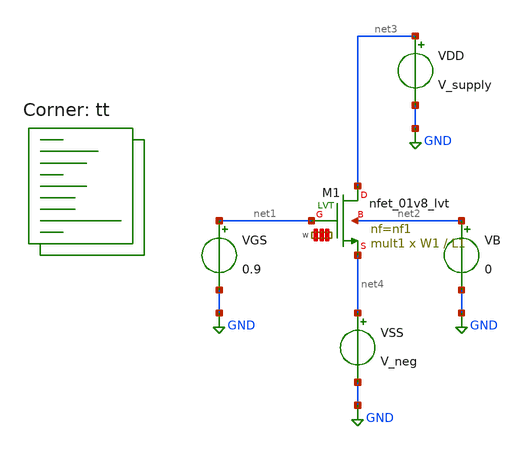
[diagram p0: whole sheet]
** sch_path: automatization_analog_design/mos_dc_characteristic/test.sch
**.subckt test
XM1 net3 net1 net4 net2 sky130_fd_pr__nfet_01v8_lvt L=L1 W='W1 * nf1 ' nf=nf1 ad='int((nf1 + 1)/2) * W1 / nf1 * 0.29'
+ as='int((nf1 + 2)/2) * W1 / nf1 * 0.29' pd='2*int((nf1 + 1)/2) * (W1 / nf1 + 0.29)' ps='2*int((nf1 + 2)/2) * (W1 / nf1 + 0.29)'
+ nrd='0.29 / W1 ' nrs='0.29 / W1 ' sa=0 sb=0 sd=0 mult=mult1 m=mult1
VGS net1 GND 0.9
VB net2 GND 0
VDD net3 GND V_supply
VSS net4 GND V_neg
**** begin user architecture code
.lib $::SKYWATER_MODELS/sky130.lib.spice tt
**** end user architecture code
**.ends
.GLOBAL GND
**** begin user architecture code


* ngspice commands
.options savecurrents
.TEMP 27

.param V_supply=1.8
.param V_neg=0

.param L1 = 0.15
.param W1 = 1
.param nf1=1
.param mult1=1

.control
dc VGS 0 1.8 0.0001

plot @m.xm1.msky130_fd_pr__nfet_01v8_lvt[id]
plot deriv(@m.xm1.msky130_fd_pr__nfet_01v8_lvt[id])
wrdata /home/vasco/Desktop/variation.txt @m.xm1.msky130_fd_pr__nfet_01v8_lvt[id]
+ deriv(@m.xm1.msky130_fd_pr__nfet_01v8_lvt[id])


save all
.endc



**** end user architecture code
.end
